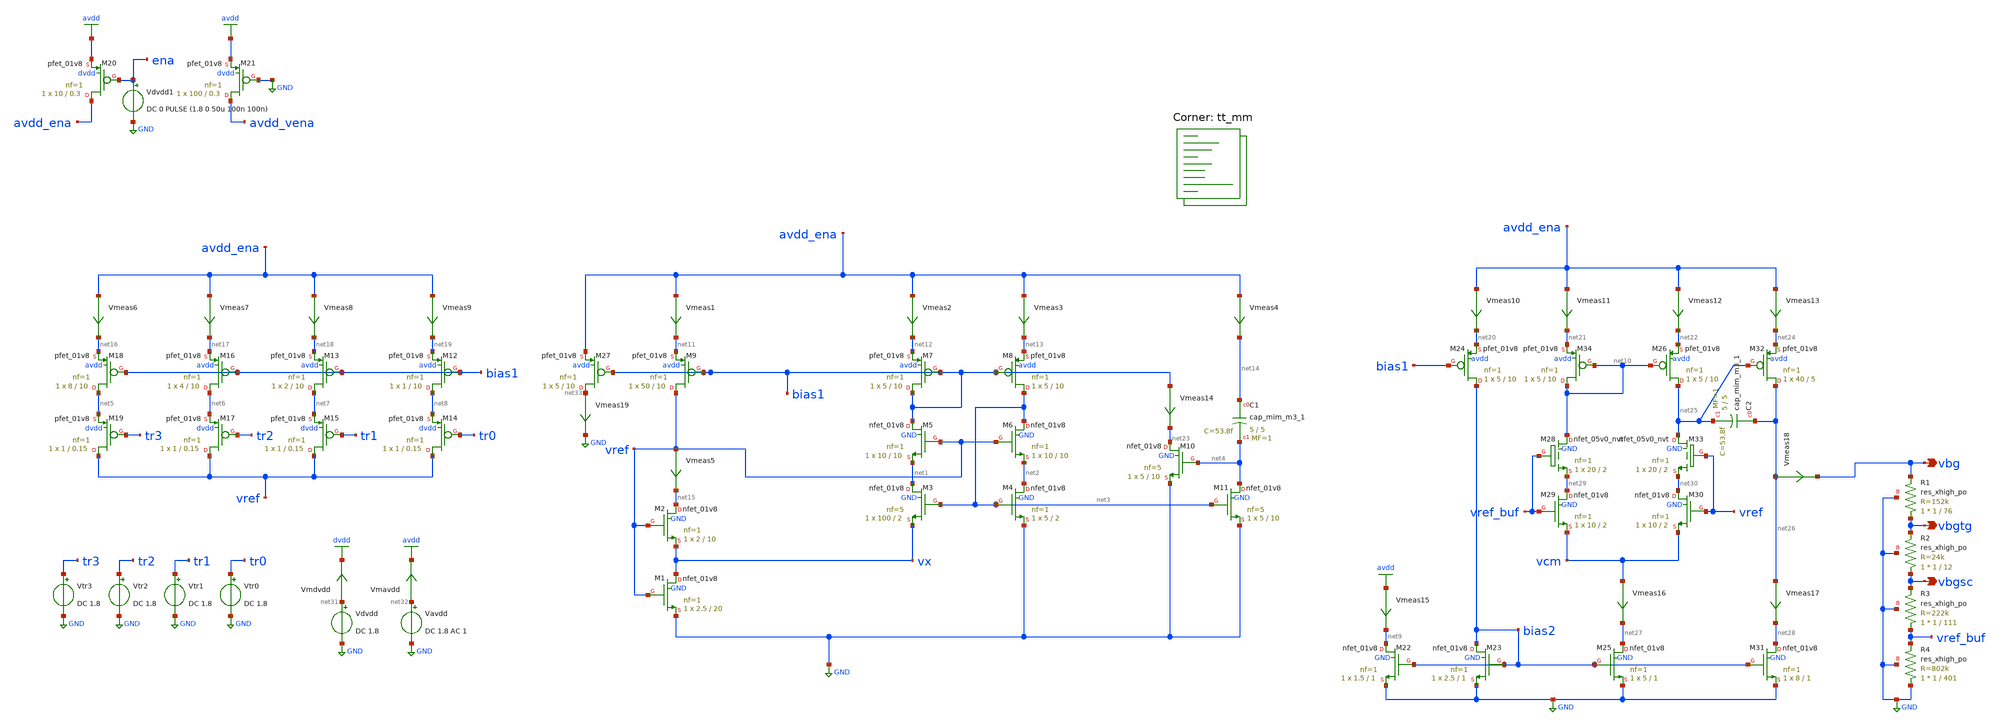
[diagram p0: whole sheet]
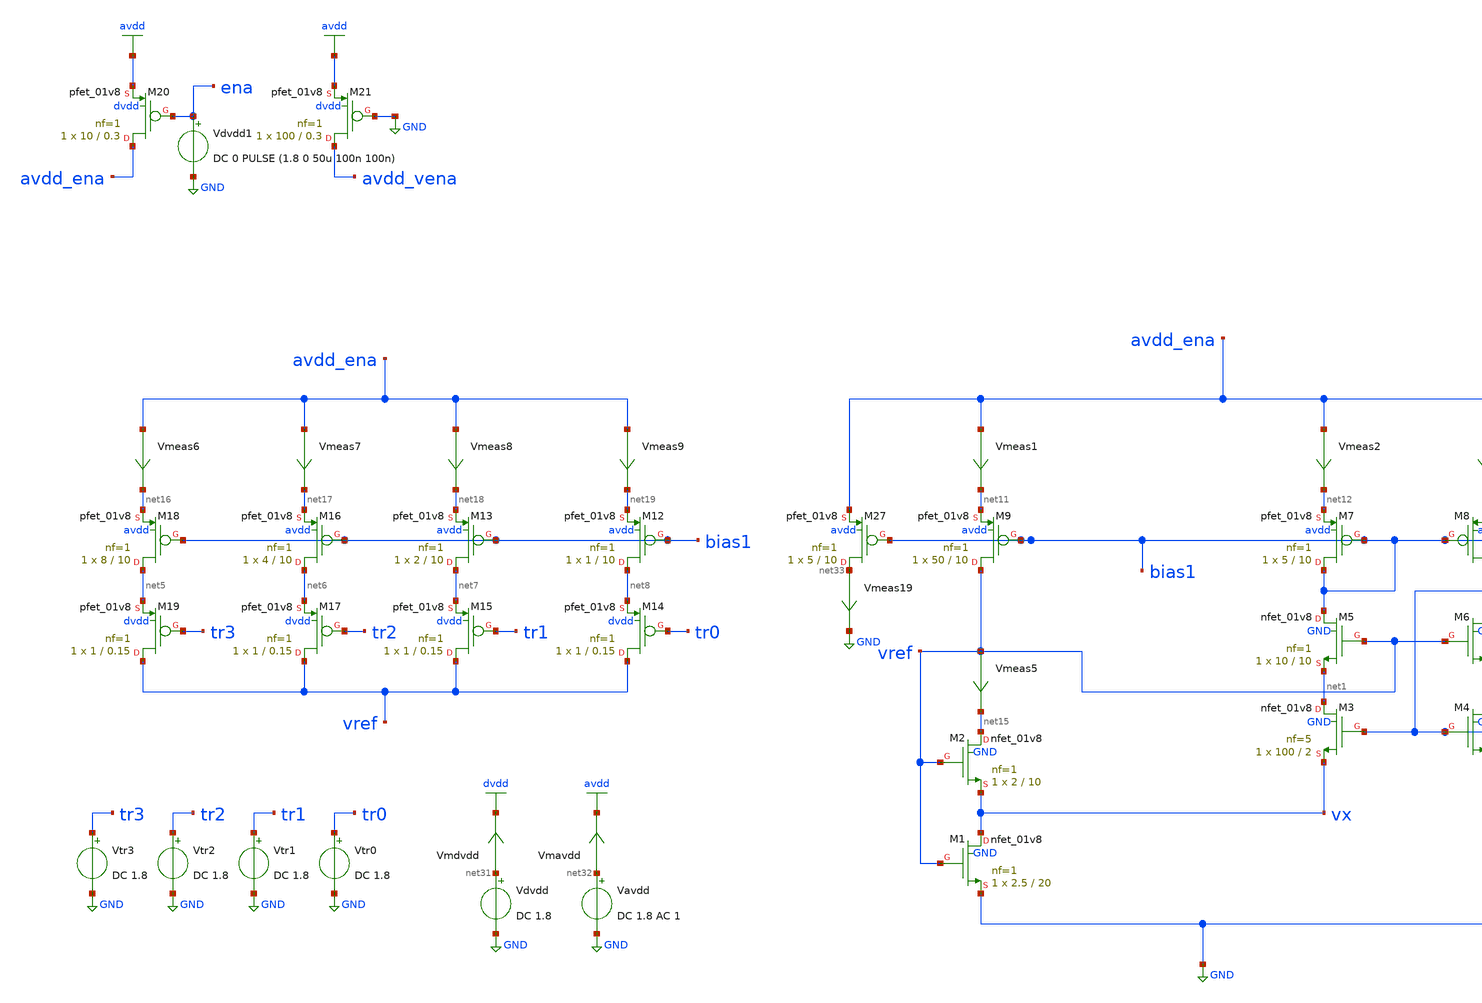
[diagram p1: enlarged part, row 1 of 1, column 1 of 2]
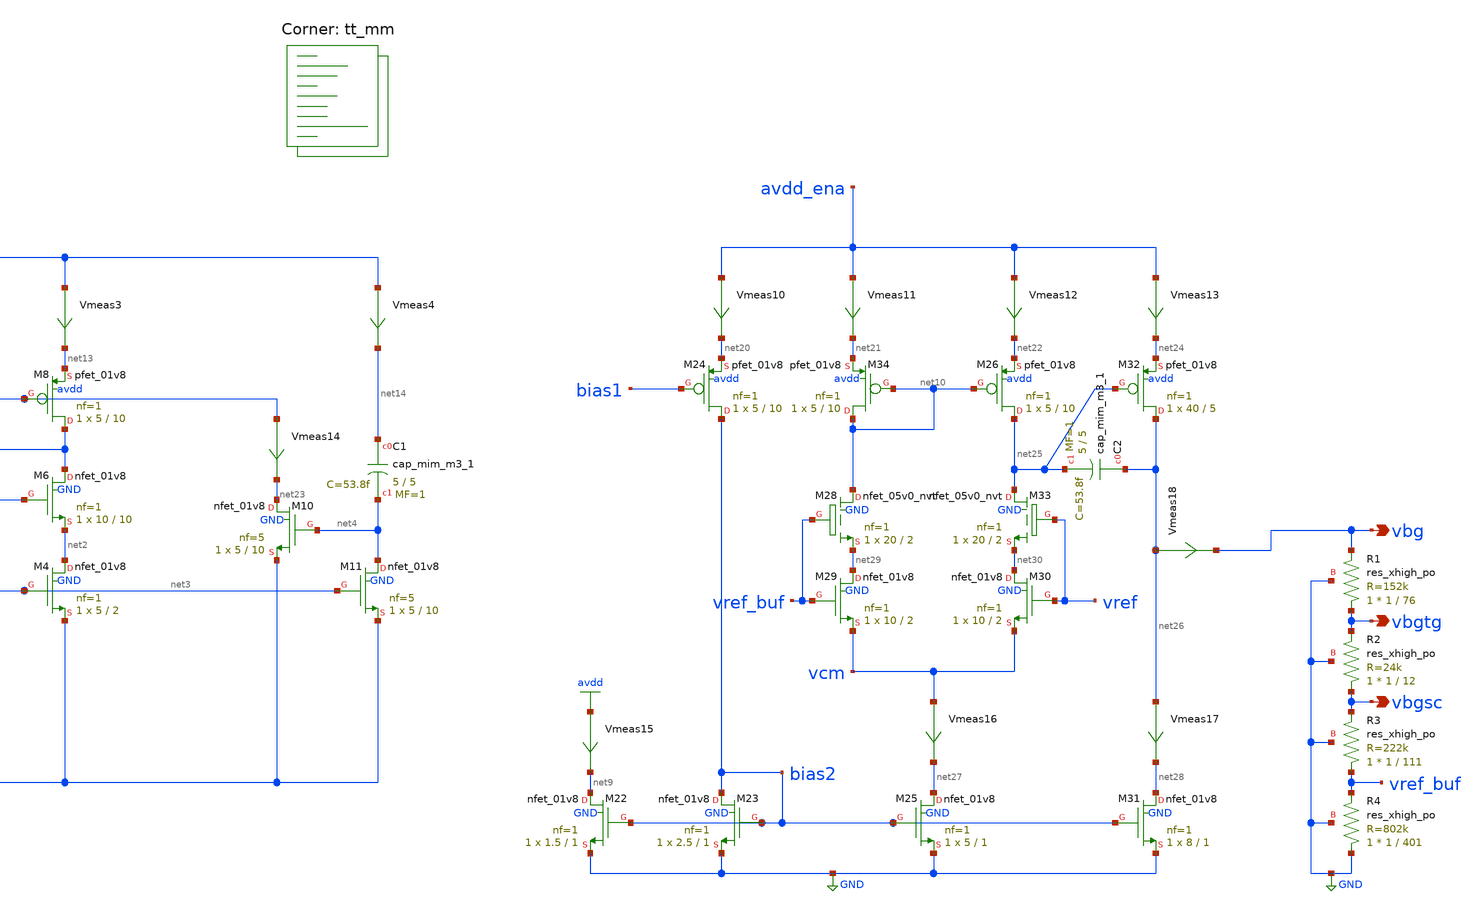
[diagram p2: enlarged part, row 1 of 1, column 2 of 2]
** sch_path: xschem/cmos_vref_design.sch
**.subckt cmos_vref_design vbg vbgsc vbgtg
*.opin vbg
*.opin vbgsc
*.opin vbgtg
XM2 net15 vref vx GND sky130_fd_pr__nfet_01v8 L=10 W=2 nf=1 ad='int((nf+1)/2) * W/nf * 0.29' as='int((nf+2)/2) * W/nf * 0.29'
+ pd='2*int((nf+1)/2) * (W/nf + 0.29)' ps='2*int((nf+2)/2) * (W/nf + 0.29)' nrd='0.29 / W' nrs='0.29 / W'
+ sa=0 sb=0 sd=0 mult=1 m=1
XM1 vx vref GND GND sky130_fd_pr__nfet_01v8 L=20 W=2.5 nf=1 ad='int((nf+1)/2) * W/nf * 0.29' as='int((nf+2)/2) * W/nf * 0.29'
+ pd='2*int((nf+1)/2) * (W/nf + 0.29)' ps='2*int((nf+2)/2) * (W/nf + 0.29)' nrd='0.29 / W' nrs='0.29 / W'
+ sa=0 sb=0 sd=0 mult=1 m=1
XM3 net1 net3 vx GND sky130_fd_pr__nfet_01v8 L=2 W=100 nf=5 ad='int((nf+1)/2) * W/nf * 0.29' as='int((nf+2)/2) * W/nf * 0.29'
+ pd='2*int((nf+1)/2) * (W/nf + 0.29)' ps='2*int((nf+2)/2) * (W/nf + 0.29)' nrd='0.29 / W' nrs='0.29 / W'
+ sa=0 sb=0 sd=0 mult=1 m=1
XM4 net2 net3 GND GND sky130_fd_pr__nfet_01v8 L=2 W=5 nf=1 ad='int((nf+1)/2) * W/nf * 0.29' as='int((nf+2)/2) * W/nf * 0.29'
+ pd='2*int((nf+1)/2) * (W/nf + 0.29)' ps='2*int((nf+2)/2) * (W/nf + 0.29)' nrd='0.29 / W' nrs='0.29 / W'
+ sa=0 sb=0 sd=0 mult=1 m=1
XM5 bias1 vref net1 GND sky130_fd_pr__nfet_01v8 L=10 W=10 nf=1 ad='int((nf+1)/2) * W/nf * 0.29' as='int((nf+2)/2) * W/nf * 0.29'
+ pd='2*int((nf+1)/2) * (W/nf + 0.29)' ps='2*int((nf+2)/2) * (W/nf + 0.29)' nrd='0.29 / W' nrs='0.29 / W'
+ sa=0 sb=0 sd=0 mult=1 m=1
XM6 net3 vref net2 GND sky130_fd_pr__nfet_01v8 L=10 W=10 nf=1 ad='int((nf+1)/2) * W/nf * 0.29' as='int((nf+2)/2) * W/nf * 0.29'
+ pd='2*int((nf+1)/2) * (W/nf + 0.29)' ps='2*int((nf+2)/2) * (W/nf + 0.29)' nrd='0.29 / W' nrs='0.29 / W'
+ sa=0 sb=0 sd=0 mult=1 m=1
XM7 bias1 bias1 net12 avdd sky130_fd_pr__pfet_01v8 L=10 W=5 nf=1 ad='int((nf+1)/2) * W/nf * 0.29' as='int((nf+2)/2) * W/nf * 0.29'
+ pd='2*int((nf+1)/2) * (W/nf + 0.29)' ps='2*int((nf+2)/2) * (W/nf + 0.29)' nrd='0.29 / W' nrs='0.29 / W'
+ sa=0 sb=0 sd=0 mult=1 m=1
XM8 net3 bias1 net13 avdd sky130_fd_pr__pfet_01v8 L=10 W=5 nf=1 ad='int((nf+1)/2) * W/nf * 0.29' as='int((nf+2)/2) * W/nf * 0.29'
+ pd='2*int((nf+1)/2) * (W/nf + 0.29)' ps='2*int((nf+2)/2) * (W/nf + 0.29)' nrd='0.29 / W' nrs='0.29 / W'
+ sa=0 sb=0 sd=0 mult=1 m=1
XM9 vref bias1 net11 avdd sky130_fd_pr__pfet_01v8 L=10 W=50 nf=1 ad='int((nf+1)/2) * W/nf * 0.29' as='int((nf+2)/2) * W/nf * 0.29'
+ pd='2*int((nf+1)/2) * (W/nf + 0.29)' ps='2*int((nf+2)/2) * (W/nf + 0.29)' nrd='0.29 / W' nrs='0.29 / W'
+ sa=0 sb=0 sd=0 mult=1 m=1
XM12 net8 bias1 net19 avdd sky130_fd_pr__pfet_01v8 L=10 W=1 nf=1 ad='int((nf+1)/2) * W/nf * 0.29' as='int((nf+2)/2) * W/nf * 0.29'
+ pd='2*int((nf+1)/2) * (W/nf + 0.29)' ps='2*int((nf+2)/2) * (W/nf + 0.29)' nrd='0.29 / W' nrs='0.29 / W'
+ sa=0 sb=0 sd=0 mult=1 m=1
XM13 net7 bias1 net18 avdd sky130_fd_pr__pfet_01v8 L=10 W=2 nf=1 ad='int((nf+1)/2) * W/nf * 0.29' as='int((nf+2)/2) * W/nf * 0.29'
+ pd='2*int((nf+1)/2) * (W/nf + 0.29)' ps='2*int((nf+2)/2) * (W/nf + 0.29)' nrd='0.29 / W' nrs='0.29 / W'
+ sa=0 sb=0 sd=0 mult=1 m=1
XM14 vref tr0 net8 dvdd sky130_fd_pr__pfet_01v8 L=0.15 W=1 nf=1 ad='int((nf+1)/2) * W/nf * 0.29' as='int((nf+2)/2) * W/nf * 0.29'
+ pd='2*int((nf+1)/2) * (W/nf + 0.29)' ps='2*int((nf+2)/2) * (W/nf + 0.29)' nrd='0.29 / W' nrs='0.29 / W'
+ sa=0 sb=0 sd=0 mult=1 m=1
XM15 vref tr1 net7 dvdd sky130_fd_pr__pfet_01v8 L=0.15 W=1 nf=1 ad='int((nf+1)/2) * W/nf * 0.29' as='int((nf+2)/2) * W/nf * 0.29'
+ pd='2*int((nf+1)/2) * (W/nf + 0.29)' ps='2*int((nf+2)/2) * (W/nf + 0.29)' nrd='0.29 / W' nrs='0.29 / W'
+ sa=0 sb=0 sd=0 mult=1 m=1
XM16 net6 bias1 net17 avdd sky130_fd_pr__pfet_01v8 L=10 W=4 nf=1 ad='int((nf+1)/2) * W/nf * 0.29' as='int((nf+2)/2) * W/nf * 0.29'
+ pd='2*int((nf+1)/2) * (W/nf + 0.29)' ps='2*int((nf+2)/2) * (W/nf + 0.29)' nrd='0.29 / W' nrs='0.29 / W'
+ sa=0 sb=0 sd=0 mult=1 m=1
XM17 vref tr2 net6 dvdd sky130_fd_pr__pfet_01v8 L=0.15 W=1 nf=1 ad='int((nf+1)/2) * W/nf * 0.29' as='int((nf+2)/2) * W/nf * 0.29'
+ pd='2*int((nf+1)/2) * (W/nf + 0.29)' ps='2*int((nf+2)/2) * (W/nf + 0.29)' nrd='0.29 / W' nrs='0.29 / W'
+ sa=0 sb=0 sd=0 mult=1 m=1
XM18 net5 bias1 net16 avdd sky130_fd_pr__pfet_01v8 L=10 W=8 nf=1 ad='int((nf+1)/2) * W/nf * 0.29' as='int((nf+2)/2) * W/nf * 0.29'
+ pd='2*int((nf+1)/2) * (W/nf + 0.29)' ps='2*int((nf+2)/2) * (W/nf + 0.29)' nrd='0.29 / W' nrs='0.29 / W'
+ sa=0 sb=0 sd=0 mult=1 m=1
XM19 vref tr3 net5 dvdd sky130_fd_pr__pfet_01v8 L=0.15 W=1 nf=1 ad='int((nf+1)/2) * W/nf * 0.29' as='int((nf+2)/2) * W/nf * 0.29'
+ pd='2*int((nf+1)/2) * (W/nf + 0.29)' ps='2*int((nf+2)/2) * (W/nf + 0.29)' nrd='0.29 / W' nrs='0.29 / W'
+ sa=0 sb=0 sd=0 mult=1 m=1
XM20 avdd_ena ena avdd dvdd sky130_fd_pr__pfet_01v8 L=0.3 W=10 nf=1 ad='int((nf+1)/2) * W/nf * 0.29'
+ as='int((nf+2)/2) * W/nf * 0.29' pd='2*int((nf+1)/2) * (W/nf + 0.29)' ps='2*int((nf+2)/2) * (W/nf + 0.29)'
+ nrd='0.29 / W' nrs='0.29 / W' sa=0 sb=0 sd=0 mult=1 m=1
XM21 avdd_vena GND avdd dvdd sky130_fd_pr__pfet_01v8 L=0.3 W=100 nf=1 ad='int((nf+1)/2) * W/nf * 0.29'
+ as='int((nf+2)/2) * W/nf * 0.29' pd='2*int((nf+1)/2) * (W/nf + 0.29)' ps='2*int((nf+2)/2) * (W/nf + 0.29)'
+ nrd='0.29 / W' nrs='0.29 / W' sa=0 sb=0 sd=0 mult=1 m=1
XM22 net9 bias2 GND GND sky130_fd_pr__nfet_01v8 L=1 W=1.5 nf=1 ad='int((nf+1)/2) * W/nf * 0.29' as='int((nf+2)/2) * W/nf * 0.29'
+ pd='2*int((nf+1)/2) * (W/nf + 0.29)' ps='2*int((nf+2)/2) * (W/nf + 0.29)' nrd='0.29 / W' nrs='0.29 / W'
+ sa=0 sb=0 sd=0 mult=1 m=1
XM23 bias2 bias2 GND GND sky130_fd_pr__nfet_01v8 L=1 W=2.5 nf=1 ad='int((nf+1)/2) * W/nf * 0.29' as='int((nf+2)/2) * W/nf * 0.29'
+ pd='2*int((nf+1)/2) * (W/nf + 0.29)' ps='2*int((nf+2)/2) * (W/nf + 0.29)' nrd='0.29 / W' nrs='0.29 / W'
+ sa=0 sb=0 sd=0 mult=1 m=1
XM24 bias2 bias1 net20 avdd sky130_fd_pr__pfet_01v8 L=10 W=5 nf=1 ad='int((nf+1)/2) * W/nf * 0.29' as='int((nf+2)/2) * W/nf * 0.29'
+ pd='2*int((nf+1)/2) * (W/nf + 0.29)' ps='2*int((nf+2)/2) * (W/nf + 0.29)' nrd='0.29 / W' nrs='0.29 / W'
+ sa=0 sb=0 sd=0 mult=1 m=1
XM25 net27 bias2 GND GND sky130_fd_pr__nfet_01v8 L=1 W=5 nf=1 ad='int((nf+1)/2) * W/nf * 0.29' as='int((nf+2)/2) * W/nf * 0.29'
+ pd='2*int((nf+1)/2) * (W/nf + 0.29)' ps='2*int((nf+2)/2) * (W/nf + 0.29)' nrd='0.29 / W' nrs='0.29 / W'
+ sa=0 sb=0 sd=0 mult=1 m=1
XM26 net25 net10 net22 avdd sky130_fd_pr__pfet_01v8 L=10 W=5 nf=1 ad='int((nf+1)/2) * W/nf * 0.29' as='int((nf+2)/2) * W/nf * 0.29'
+ pd='2*int((nf+1)/2) * (W/nf + 0.29)' ps='2*int((nf+2)/2) * (W/nf + 0.29)' nrd='0.29 / W' nrs='0.29 / W'
+ sa=0 sb=0 sd=0 mult=1 m=1
XM29 net29 vref_buf vcm GND sky130_fd_pr__nfet_01v8 L=2 W=10 nf=1 ad='int((nf+1)/2) * W/nf * 0.29' as='int((nf+2)/2) * W/nf * 0.29'
+ pd='2*int((nf+1)/2) * (W/nf + 0.29)' ps='2*int((nf+2)/2) * (W/nf + 0.29)' nrd='0.29 / W' nrs='0.29 / W'
+ sa=0 sb=0 sd=0 mult=1 m=1
XM30 net30 vref vcm GND sky130_fd_pr__nfet_01v8 L=2 W=10 nf=1 ad='int((nf+1)/2) * W/nf * 0.29' as='int((nf+2)/2) * W/nf * 0.29'
+ pd='2*int((nf+1)/2) * (W/nf + 0.29)' ps='2*int((nf+2)/2) * (W/nf + 0.29)' nrd='0.29 / W' nrs='0.29 / W'
+ sa=0 sb=0 sd=0 mult=1 m=1
XM34 net10 net10 net21 avdd sky130_fd_pr__pfet_01v8 L=10 W=5 nf=1 ad='int((nf+1)/2) * W/nf * 0.29' as='int((nf+2)/2) * W/nf * 0.29'
+ pd='2*int((nf+1)/2) * (W/nf + 0.29)' ps='2*int((nf+2)/2) * (W/nf + 0.29)' nrd='0.29 / W' nrs='0.29 / W'
+ sa=0 sb=0 sd=0 mult=1 m=1
XM10 net23 net4 GND GND sky130_fd_pr__nfet_01v8 L=10 W=5 nf=5 ad='int((nf+1)/2) * W/nf * 0.29' as='int((nf+2)/2) * W/nf * 0.29'
+ pd='2*int((nf+1)/2) * (W/nf + 0.29)' ps='2*int((nf+2)/2) * (W/nf + 0.29)' nrd='0.29 / W' nrs='0.29 / W'
+ sa=0 sb=0 sd=0 mult=1 m=1
XM11 net4 net3 GND GND sky130_fd_pr__nfet_01v8 L=10 W=5 nf=5 ad='int((nf+1)/2) * W/nf * 0.29' as='int((nf+2)/2) * W/nf * 0.29'
+ pd='2*int((nf+1)/2) * (W/nf + 0.29)' ps='2*int((nf+2)/2) * (W/nf + 0.29)' nrd='0.29 / W' nrs='0.29 / W'
+ sa=0 sb=0 sd=0 mult=1 m=1
XC1 net14 net4 sky130_fd_pr__cap_mim_m3_1 W=5 L=5 MF=1 m=1
Vmeas1 avdd_ena net11 0
.save i(vmeas1)
Vmeas2 avdd_ena net12 0
.save i(vmeas2)
Vmeas3 avdd_ena net13 0
.save i(vmeas3)
Vmeas4 avdd_ena net14 0
.save i(vmeas4)
Vmeas5 vref net15 0
.save i(vmeas5)
Vmeas6 avdd_ena net16 0
.save i(vmeas6)
Vmeas7 avdd_ena net17 0
.save i(vmeas7)
Vmeas8 avdd_ena net18 0
.save i(vmeas8)
Vmeas9 avdd_ena net19 0
.save i(vmeas9)
Vmeas10 avdd_ena net20 0
.save i(vmeas10)
Vmeas11 avdd_ena net21 0
.save i(vmeas11)
Vmeas12 avdd_ena net22 0
.save i(vmeas12)
Vmeas13 avdd_ena net24 0
.save i(vmeas13)
Vdvdd net31 GND DC 1.8
Vavdd net32 GND DC 1.8 AC 1
Vtr0 tr0 GND DC 1.8
Vtr1 tr1 GND DC 1.8
Vtr2 tr2 GND DC 1.8
Vtr3 tr3 GND DC 1.8
Vmeas14 bias1 net23 0
.save i(vmeas14)
XM31 net28 bias2 GND GND sky130_fd_pr__nfet_01v8 L=1 W=8 nf=1 ad='int((nf+1)/2) * W/nf * 0.29' as='int((nf+2)/2) * W/nf * 0.29'
+ pd='2*int((nf+1)/2) * (W/nf + 0.29)' ps='2*int((nf+2)/2) * (W/nf + 0.29)' nrd='0.29 / W' nrs='0.29 / W'
+ sa=0 sb=0 sd=0 mult=1 m=1
XC2 net26 net25 sky130_fd_pr__cap_mim_m3_1 W=5 L=5 MF=1 m=1
XM32 net26 net25 net24 avdd sky130_fd_pr__pfet_01v8 L=5 W=40 nf=1 ad='int((nf+1)/2) * W/nf * 0.29' as='int((nf+2)/2) * W/nf * 0.29'
+ pd='2*int((nf+1)/2) * (W/nf + 0.29)' ps='2*int((nf+2)/2) * (W/nf + 0.29)' nrd='0.29 / W' nrs='0.29 / W'
+ sa=0 sb=0 sd=0 mult=1 m=1
Vmeas15 avdd net9 0
.save i(vmeas15)
Vmeas16 vcm net27 0
.save i(vmeas16)
Vmeas17 net26 net28 0
.save i(vmeas17)
Vmeas18 net26 vbg 0
.save i(vmeas18)
Vmavdd net32 avdd 0
.save i(vmavdd)
Vmdvdd net31 dvdd 0
.save i(vmdvdd)
Vdvdd1 ena GND DC 0 PULSE (1.8 0 50u 100n 100n)
XM27 net33 bias1 avdd_ena avdd sky130_fd_pr__pfet_01v8 L=10 W=5 nf=1 ad='int((nf+1)/2) * W/nf * 0.29'
+ as='int((nf+2)/2) * W/nf * 0.29' pd='2*int((nf+1)/2) * (W/nf + 0.29)' ps='2*int((nf+2)/2) * (W/nf + 0.29)'
+ nrd='0.29 / W' nrs='0.29 / W' sa=0 sb=0 sd=0 mult=1 m=1
Vmeas19 net33 GND 0
.save i(vmeas19)
XM28 net10 vref_buf net29 GND sky130_fd_pr__nfet_05v0_nvt L=2 W=20 nf=1 ad='int((nf+1)/2) * W/nf * 0.29'
+ as='int((nf+2)/2) * W/nf * 0.29' pd='2*int((nf+1)/2) * (W/nf + 0.29)' ps='2*int((nf+2)/2) * (W/nf + 0.29)'
+ nrd='0.29 / W' nrs='0.29 / W' sa=0 sb=0 sd=0 mult=1 m=1
XM33 net25 vref net30 GND sky130_fd_pr__nfet_05v0_nvt L=2 W=20 nf=1 ad='int((nf+1)/2) * W/nf * 0.29'
+ as='int((nf+2)/2) * W/nf * 0.29' pd='2*int((nf+1)/2) * (W/nf + 0.29)' ps='2*int((nf+2)/2) * (W/nf + 0.29)'
+ nrd='0.29 / W' nrs='0.29 / W' sa=0 sb=0 sd=0 mult=1 m=1
XR4 GND vref_buf GND sky130_fd_pr__res_xhigh_po W=1 L=401 mult=1 m=1
XR3 vref_buf vbgsc GND sky130_fd_pr__res_xhigh_po W=1 L=111 mult=1 m=1
XR2 vbgsc vbgtg GND sky130_fd_pr__res_xhigh_po W=1 L=12 mult=1 m=1
XR1 vbgtg vbg GND sky130_fd_pr__res_xhigh_po W=1 L=76 mult=1 m=1
**** begin user architecture code
.lib $::SKYWATER_MODELS/sky130.lib.spice tt_mm


.option warn=1
.control
save all
*op
*write vrefdesign_op.raw
dc TEMP -40 85 5
*dc Vavdd 0 1.92 50m
*tran 10n 100us 50us
*plot i(vmeas1)
*plot i(vmavdd), i(vmdvdd)
plot vref_buf, vref
plot vref_buf-vref
*write vrefdesign_tempsweep.raw
*noise v(vref_buf) Vavdd dec 10 0.1 10
*setplot noise2
*print onoise_total
.endc


**** end user architecture code
**.ends
.GLOBAL GND
.GLOBAL avdd
.GLOBAL dvdd
.end
